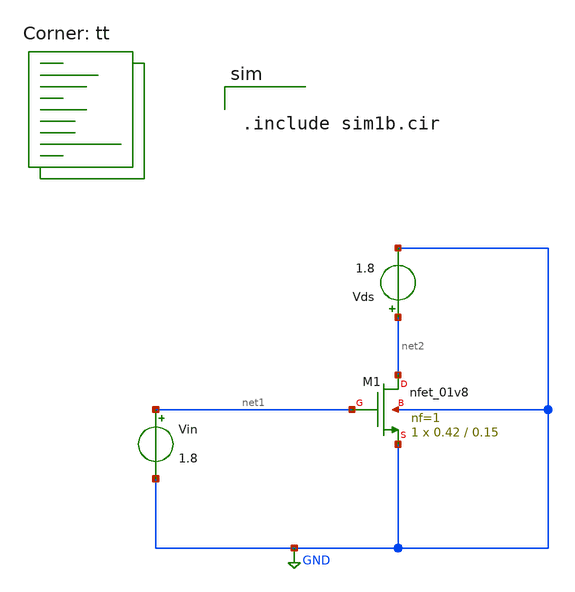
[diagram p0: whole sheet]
** sch_path: assignments/assignment1/assign1b.sch
**.subckt assign1b
Vin net1 GND 1.8
XM1 net2 net1 GND GND sky130_fd_pr__nfet_01v8 L=0.15 W=0.42 nf=1 ad='int((nf+1)/2) * W/nf * 0.29' as='int((nf+2)/2) * W/nf * 0.29'
+ pd='2*int((nf+1)/2) * (W/nf + 0.29)' ps='2*int((nf+2)/2) * (W/nf + 0.29)' nrd='0.29 / W' nrs='0.29 / W'
+ sa=0 sb=0 sd=0 mult=1 m=1
Vds net2 GND 1.8
**** begin user architecture code


.include sim1b.cir


.lib $::SKYWATER_MODELS/sky130.lib.spice tt
**** end user architecture code
**.ends
.GLOBAL GND
.end
